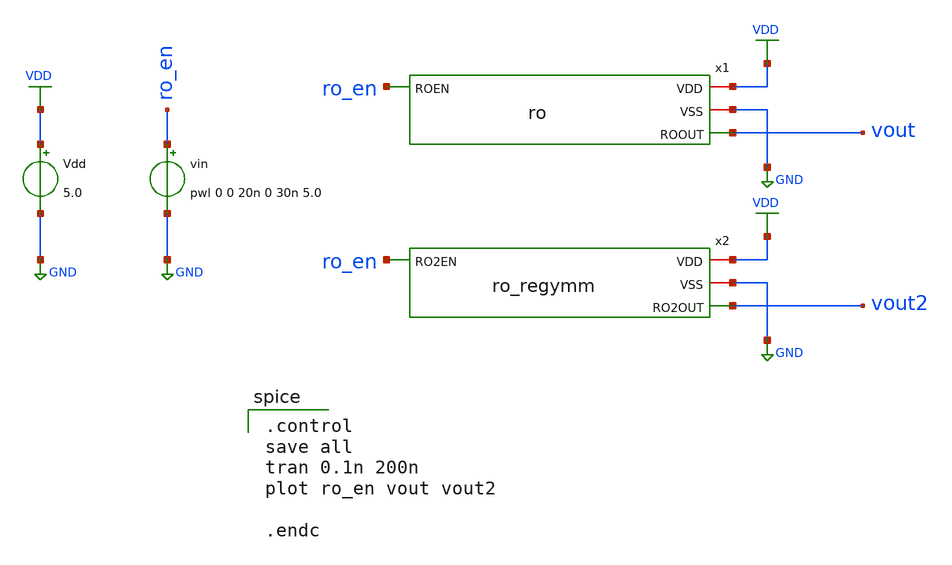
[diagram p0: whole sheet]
** sch_path: src/ro_tb.sch
**.subckt ro_tb
vin ro_en GND pwl 0 0 20n 0 30n 5.0
Vdd VDD GND 5.0
x1 VDD GND ro_en vout ro
x2 VDD GND ro_en vout2 ro_regymm
**** begin user architecture code

.control
save all
tran 0.1n 200n
plot ro_en vout vout2

.endc

 .include $::LIB/ip62_models
**** end user architecture code
**.ends
.GLOBAL VDD
.GLOBAL GND
.end
